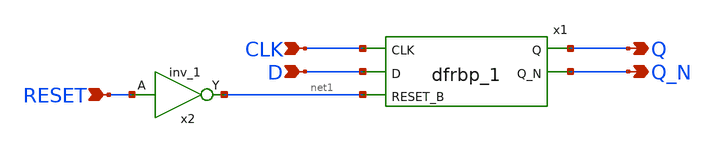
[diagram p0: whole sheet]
** sch_path: xschem/df4.sch
**.subckt df4 CLK D RESET Q Q_N
*.ipin CLK
*.ipin D
*.ipin RESET
*.opin Q
*.opin Q_N
x2 RESET GND GND VDD VDD net1 sky130_fd_sc_hd__inv_1
x1 CLK D net1 GND GND VDD VDD Q Q_N sky130_fd_sc_hd__dfrbp_1
**.ends
.end
